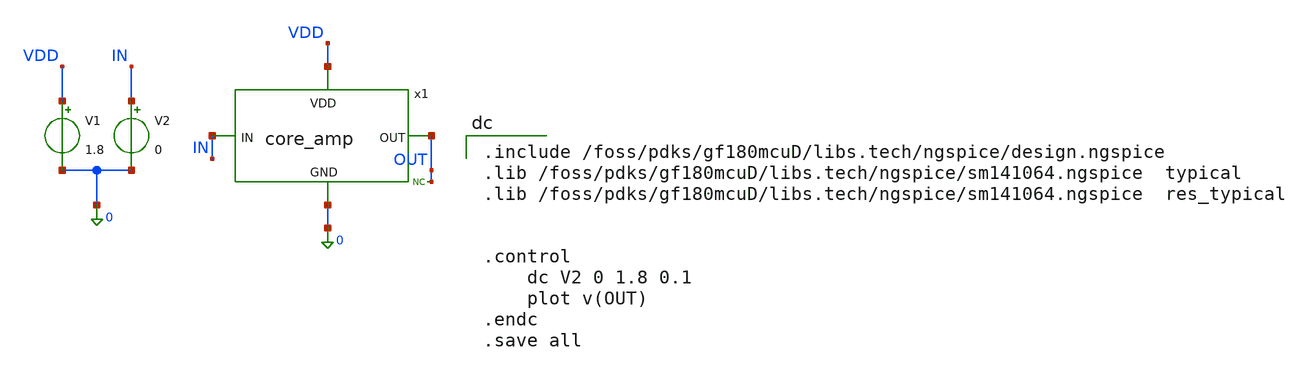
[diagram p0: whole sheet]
** sch_path: core_amp_test.sch
**.subckt core_amp_test
x1 IN OUT VDD 0 core_amp
V1 VDD 0 1.8
V2 IN 0 0
* noconn OUT
**** begin user architecture code

.include /foss/pdks/gf180mcuD/libs.tech/ngspice/design.ngspice
.lib /foss/pdks/gf180mcuD/libs.tech/ngspice/sm141064.ngspice  typical
.lib /foss/pdks/gf180mcuD/libs.tech/ngspice/sm141064.ngspice  res_typical


.control
	dc V2 0 1.8 0.1
	plot v(OUT)
.endc
.save all


**** end user architecture code
**.ends

* expanding   symbol:  core_amp.sym # of pins=4
** sym_path: core_amp.sym
** sch_path: core_amp.sch
.subckt core_amp IN OUT VDD GND
*.ipin IN
*.opin OUT
*.iopin VDD
*.iopin GND
XM1 OUT IN GND GND nfet_03v3 L=0.28u W=10u nf=1 ad='int((nf+1)/2) * W/nf * 0.18u' as='int((nf+2)/2) * W/nf * 0.18u'
+ pd='2*int((nf+1)/2) * (W/nf + 0.18u)' ps='2*int((nf+2)/2) * (W/nf + 0.18u)' nrd='0.18u / W' nrs='0.18u / W'
+ sa=0 sb=0 sd=0 m=1
XM2 OUT net1 VDD VDD pfet_03v3 L=2.5u W=1u nf=1 ad='int((nf+1)/2) * W/nf * 0.18u' as='int((nf+2)/2) * W/nf * 0.18u'
+ pd='2*int((nf+1)/2) * (W/nf + 0.18u)' ps='2*int((nf+2)/2) * (W/nf + 0.18u)' nrd='0.18u / W' nrs='0.18u / W'
+ sa=0 sb=0 sd=0 m=1
XM3 net1 net1 VDD VDD pfet_03v3 L=2.5u W=1u nf=1 ad='int((nf+1)/2) * W/nf * 0.18u' as='int((nf+2)/2) * W/nf * 0.18u'
+ pd='2*int((nf+1)/2) * (W/nf + 0.18u)' ps='2*int((nf+2)/2) * (W/nf + 0.18u)' nrd='0.18u / W' nrs='0.18u / W'
+ sa=0 sb=0 sd=0 m=1
XR1 GND net1 VDD ppolyf_u_1k r_width=2e-6 r_length=3e-6 m=10
.ends

.end
